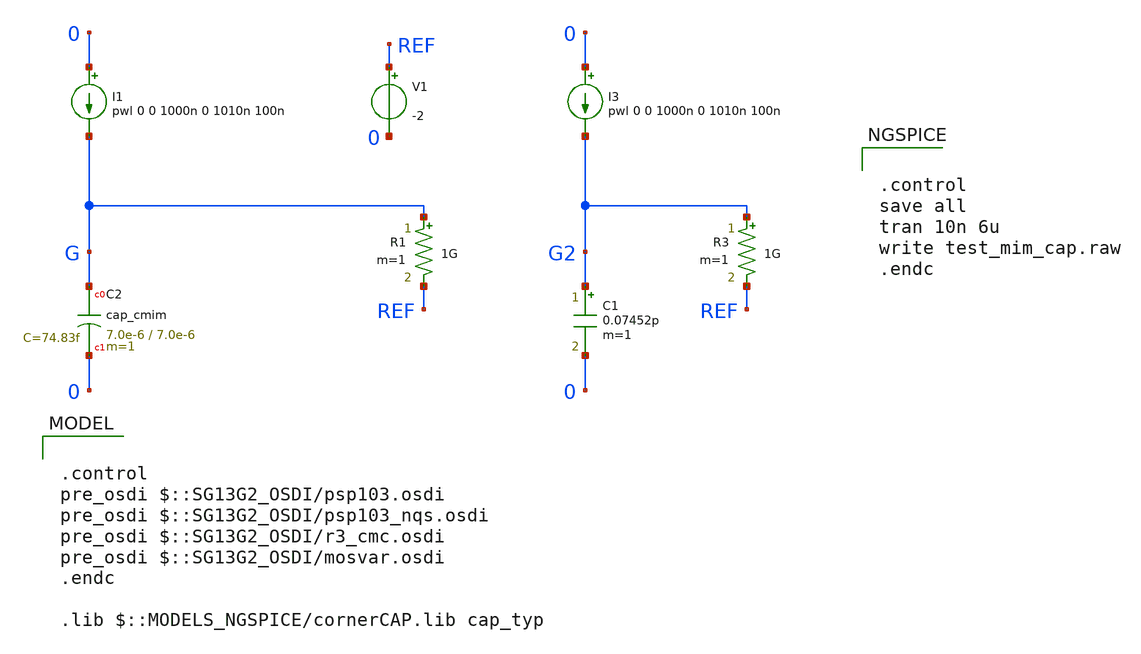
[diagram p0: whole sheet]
** sch_path: ihp-sg13g2/xschem_libs/sg13g2_tests/tran_mim_cap/schematic/tran_mim_cap.sch
* Copyright 2021 Stefan Frederik Schippers
* Licensed under the Apache License, Version 2.0 (the "License");
* you may not use this file except in compliance with the License.
* You may obtain a copy of the License at
* https://www.apache.org/licenses/LICENSE-2.0
* Unless required by applicable law or agreed to in writing, software
* distributed under the License is distributed on an "AS IS" BASIS,
* WITHOUT WARRANTIES OR CONDITIONS OF ANY KIND, either express or implied.
* See the License for the specific language governing permissions and
* limitations under the License.
* Copyright 2023 IHP PDK Authors
**.subckt tran_mim_cap
I1 0 G pwl 0 0 1000n 0 1010n 100n
R1 G REF 1G m=1
I3 0 G2 pwl 0 0 1000n 0 1010n 100n
R3 G2 REF 1G m=1
C1 G2 0 0.07452p m=1
V1 REF 0 -2
XC2 G 0 cap_cmim w=7.0e-6 l=7.0e-6 m=1 mm_ok=1
**** begin user architecture code


.control
save all
tran 10n 6u
write test_mim_cap.raw
.endc



.control
pre_osdi $::SG13G2_OSDI/psp103.osdi
pre_osdi $::SG13G2_OSDI/psp103_nqs.osdi
pre_osdi $::SG13G2_OSDI/r3_cmc.osdi
pre_osdi $::SG13G2_OSDI/mosvar.osdi
.endc

.lib $::MODELS_NGSPICE/cornerCAP.lib cap_typ

**** end user architecture code
**.ends
.end
